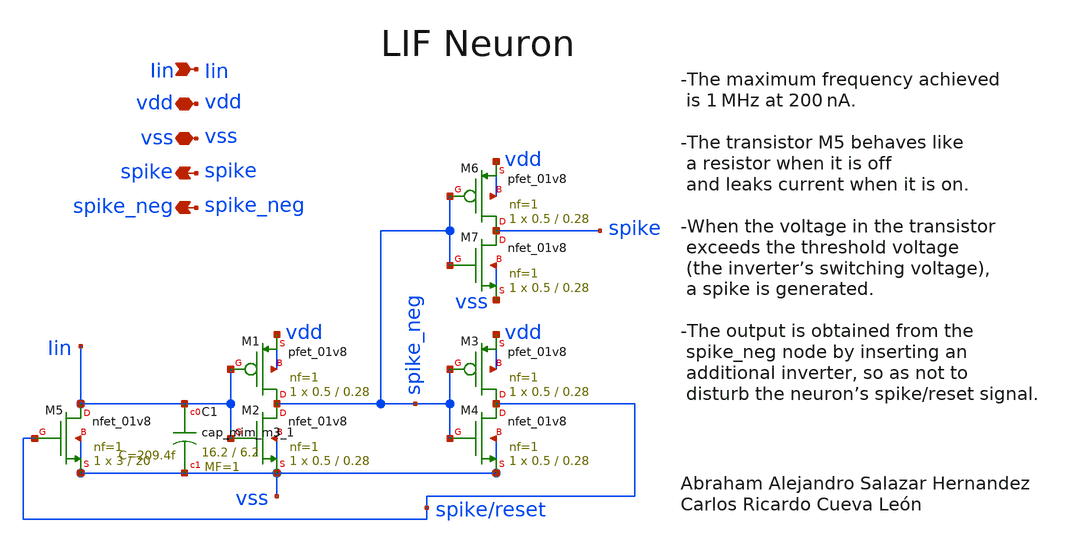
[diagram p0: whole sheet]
** sch_path: designs/libs/snn_analog/lif/sch/neurona.sch
**.subckt neurona vdd vss Iin spike spike_neg
*.iopin vdd
*.iopin vss
*.ipin Iin
*.opin spike
*.opin spike_neg
XM2 spike_neg Iin vss vss sky130_fd_pr__nfet_01v8 L=0.28 W=0.5 nf=1 ad='int((1 + 1)/2) * 0.5 / 1 * 0.29'
+ as='int((1 + 2)/2) * 0.5 / 1 * 0.29' pd='2*int((1 + 1)/2) * (0.5 / 1 + 0.29)' ps='2*int((1 + 2)/2) * (0.5 / 1 + 0.29)'
+ nrd='0.29 / 0.5 ' nrs='0.29 / 0.5 ' sa=0 sb=0 sd=0 mult=1 m=1
XM1 spike_neg Iin vdd vdd sky130_fd_pr__pfet_01v8 L=0.28 W=0.5 nf=1 ad='int((1 + 1)/2) * 0.5 / 1 * 0.29'
+ as='int((1 + 2)/2) * 0.5 / 1 * 0.29' pd='2*int((1 + 1)/2) * (0.5 / 1 + 0.29)' ps='2*int((1 + 2)/2) * (0.5 / 1 + 0.29)'
+ nrd='0.29 / 0.5 ' nrs='0.29 / 0.5 ' sa=0 sb=0 sd=0 mult=1 m=1
XM3 spike/reset spike_neg vdd vdd sky130_fd_pr__pfet_01v8 L=0.28 W=0.5 nf=1 ad='int((1 + 1)/2) * 0.5 / 1 * 0.29'
+ as='int((1 + 2)/2) * 0.5 / 1 * 0.29' pd='2*int((1 + 1)/2) * (0.5 / 1 + 0.29)' ps='2*int((1 + 2)/2) * (0.5 / 1 + 0.29)'
+ nrd='0.29 / 0.5 ' nrs='0.29 / 0.5 ' sa=0 sb=0 sd=0 mult=1 m=1
XM4 spike/reset spike_neg vss vss sky130_fd_pr__nfet_01v8 L=0.28 W=0.5 nf=1 ad='int((1 + 1)/2) * 0.5 / 1 * 0.29'
+ as='int((1 + 2)/2) * 0.5 / 1 * 0.29' pd='2*int((1 + 1)/2) * (0.5 / 1 + 0.29)' ps='2*int((1 + 2)/2) * (0.5 / 1 + 0.29)'
+ nrd='0.29 / 0.5 ' nrs='0.29 / 0.5 ' sa=0 sb=0 sd=0 mult=1 m=1
XM5 Iin spike/reset vss vss sky130_fd_pr__nfet_01v8 L=20 W=3 nf=1 ad='int((1 + 1)/2) * 3 / 1 * 0.29'
+ as='int((1 + 2)/2) * 3 / 1 * 0.29' pd='2*int((1 + 1)/2) * (3 / 1 + 0.29)' ps='2*int((1 + 2)/2) * (3 / 1 + 0.29)'
+ nrd='0.29 / 3 ' nrs='0.29 / 3 ' sa=0 sb=0 sd=0 mult=1 m=1
XM6 spike spike_neg vdd vdd sky130_fd_pr__pfet_01v8 L=0.28 W=0.5 nf=1 ad='int((1 + 1)/2) * 0.5 / 1 * 0.29'
+ as='int((1 + 2)/2) * 0.5 / 1 * 0.29' pd='2*int((1 + 1)/2) * (0.5 / 1 + 0.29)' ps='2*int((1 + 2)/2) * (0.5 / 1 + 0.29)'
+ nrd='0.29 / 0.5 ' nrs='0.29 / 0.5 ' sa=0 sb=0 sd=0 mult=1 m=1
XM7 spike spike_neg vss vss sky130_fd_pr__nfet_01v8 L=0.28 W=0.5 nf=1 ad='int((1 + 1)/2) * 0.5 / 1 * 0.29'
+ as='int((1 + 2)/2) * 0.5 / 1 * 0.29' pd='2*int((1 + 1)/2) * (0.5 / 1 + 0.29)' ps='2*int((1 + 2)/2) * (0.5 / 1 + 0.29)'
+ nrd='0.29 / 0.5 ' nrs='0.29 / 0.5 ' sa=0 sb=0 sd=0 mult=1 m=1
XC1 Iin vss sky130_fd_pr__cap_mim_m3_1 W=16.2 L=6.2 MF=1 m=1
**.ends
.end
